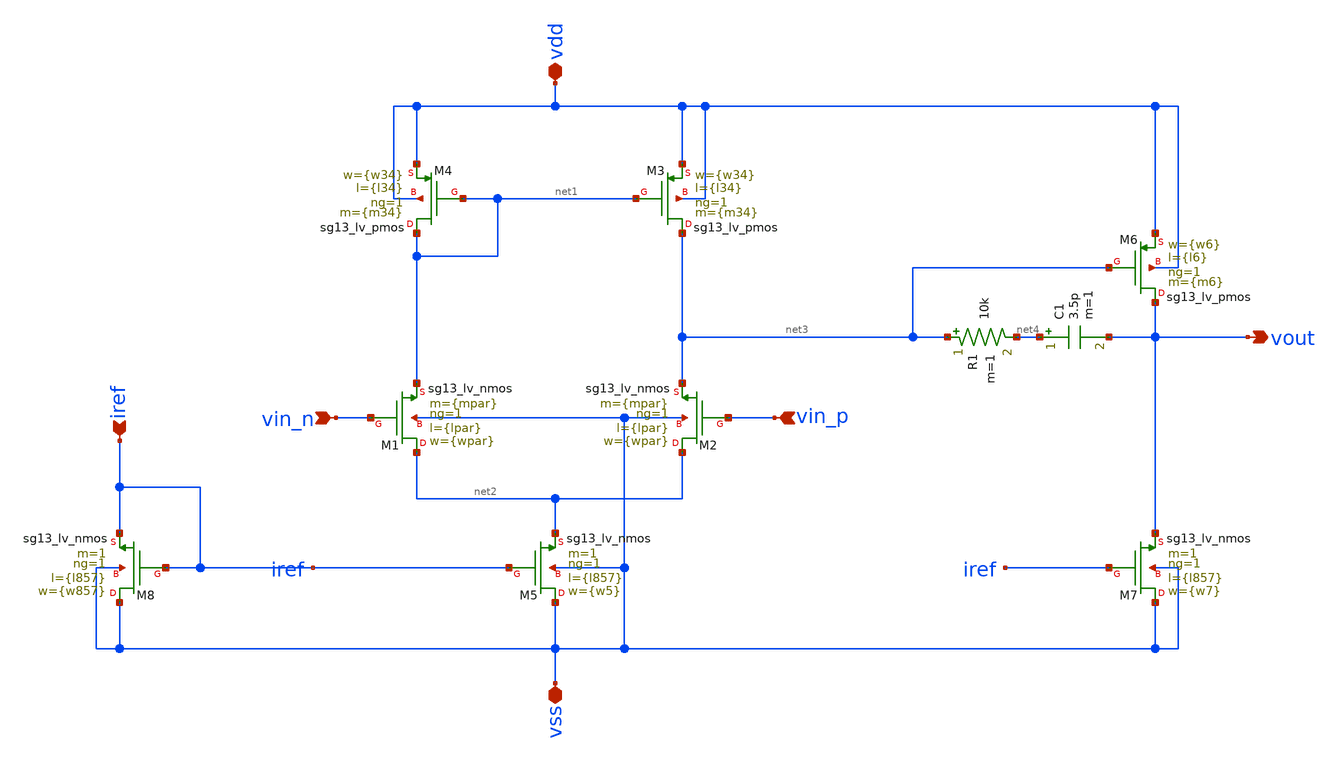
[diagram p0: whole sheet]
** sch_path: v3/ihp_ota_v3.sch
**.subckt ihp_ota_v3 iref vin_n vin_p vdd vss vout
*.ipin iref
*.ipin vin_n
*.ipin vin_p
*.iopin vdd
*.iopin vss
*.opin vout
XM1 net2 vin_n net1 vss sg13_lv_nmos w={wpar} l={lpar} ng=1 m={mpar} mm_ok=1
XM2 net2 vin_p net3 vss sg13_lv_nmos w={wpar} l={lpar} ng=1 m={mpar} mm_ok=1
XM3 net3 net1 vdd vdd sg13_lv_pmos w={w34} l={l34} ng=1 m={m34} mm_ok=1
XM4 net1 net1 vdd vdd sg13_lv_pmos w={w34} l={l34} ng=1 m={m34} mm_ok=1
XM5 vss iref net2 vss sg13_lv_nmos w={w5} l={l857} ng=1 m=1 mm_ok=1
XM8 vss iref iref vss sg13_lv_nmos w={w857} l={l857} ng=1 m=1 mm_ok=1
XM6 vout net3 vdd vdd sg13_lv_pmos w={w6} l={l6} ng=1 m={m6} mm_ok=1
XM7 vss iref vout vss sg13_lv_nmos w={w7} l={l857} ng=1 m=1 mm_ok=1
R1 net3 net4 10k m=1
C1 net4 vout 3.5p m=1
**.ends
.end
